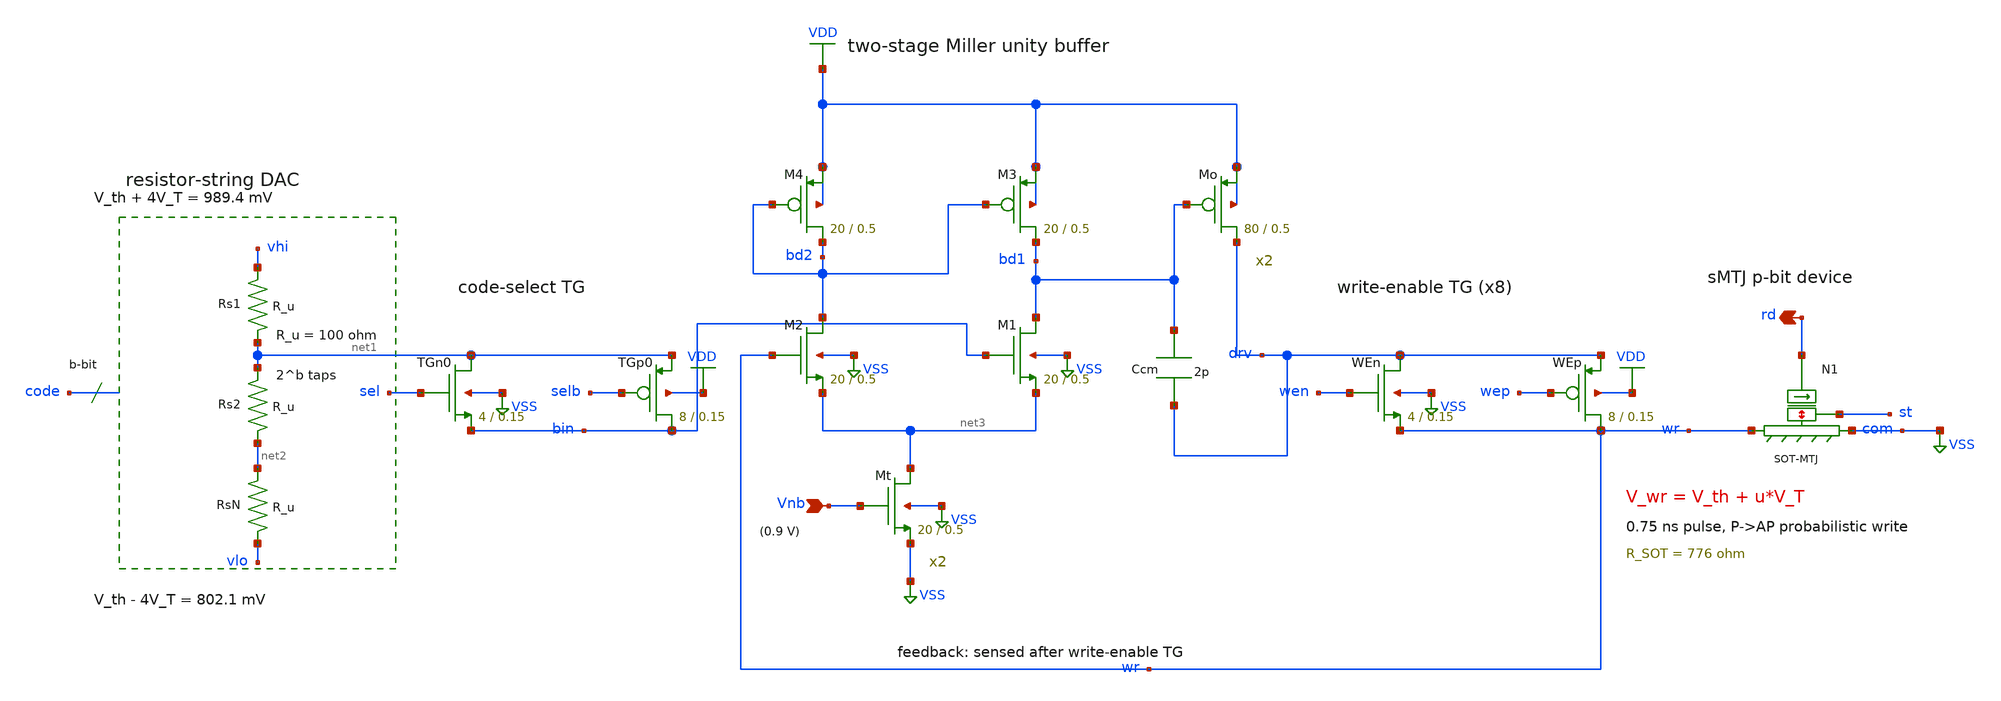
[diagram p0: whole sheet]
** sch_path: eda/schematics/update_chain.sch
**.subckt update_chain Vnb rd
*.ipin Vnb
*.opin rd
Rs1 vhi net1 R_u m=1
Rs2 net1 net2 R_u m=1
RsN net2 vlo R_u m=1
XTGn0 net1 sel bin VSS sky130_fd_pr__sky130_fd_pr__nfet_01v8 L=0.15 W=4 nrd='0.29 / W' nrs='0.29 / W'
+ sa=0 sb=0 sd=0 mult=1 m=1
XTGp0 bin selb net1 VDD sky130_fd_pr__sky130_fd_pr__pfet_01v8 L=0.15 W=8 nrd='0.29 / W' nrs='0.29 / W'
+ sa=0 sb=0 sd=0 mult=1 m=1
XM4 bd2 bd2 VDD VDD sky130_fd_pr__sky130_fd_pr__pfet_01v8 L=0.5 W=20 nrd='0.29 / W' nrs='0.29 / W' sa=0
+ sb=0 sd=0 mult=1 m=1
XM3 bd1 bd2 VDD VDD sky130_fd_pr__sky130_fd_pr__pfet_01v8 L=0.5 W=20 nrd='0.29 / W' nrs='0.29 / W' sa=0
+ sb=0 sd=0 mult=1 m=1
XM2 bd2 wr net3 VSS sky130_fd_pr__sky130_fd_pr__nfet_01v8 L=0.5 W=20 nrd='0.29 / W' nrs='0.29 / W' sa=0
+ sb=0 sd=0 mult=1 m=1
XM1 bd1 bin net3 VSS sky130_fd_pr__sky130_fd_pr__nfet_01v8 L=0.5 W=20 nrd='0.29 / W' nrs='0.29 / W' sa=0
+ sb=0 sd=0 mult=1 m=1
XMt net3 Vnb VSS VSS sky130_fd_pr__sky130_fd_pr__nfet_01v8 L=0.5 W=20 nrd='0.29 / W' nrs='0.29 / W' sa=0
+ sb=0 sd=0 mult=1 m=1
XMo drv bd1 VDD VDD sky130_fd_pr__sky130_fd_pr__pfet_01v8 L=0.5 W=80 nrd='0.29 / W' nrs='0.29 / W' sa=0
+ sb=0 sd=0 mult=1 m=1
XWEn drv wen wr VSS sky130_fd_pr__sky130_fd_pr__nfet_01v8 L=0.15 W=4 nrd='0.29 / W' nrs='0.29 / W' sa=0
+ sb=0 sd=0 mult=1 m=1
XWEp wr wep drv VDD sky130_fd_pr__sky130_fd_pr__pfet_01v8 L=0.15 W=8 nrd='0.29 / W' nrs='0.29 / W' sa=0
+ sb=0 sd=0 mult=1 m=1
Ccm bd1 drv 2p m=1
**.ends
.GLOBAL VSS
.GLOBAL VDD
.end
